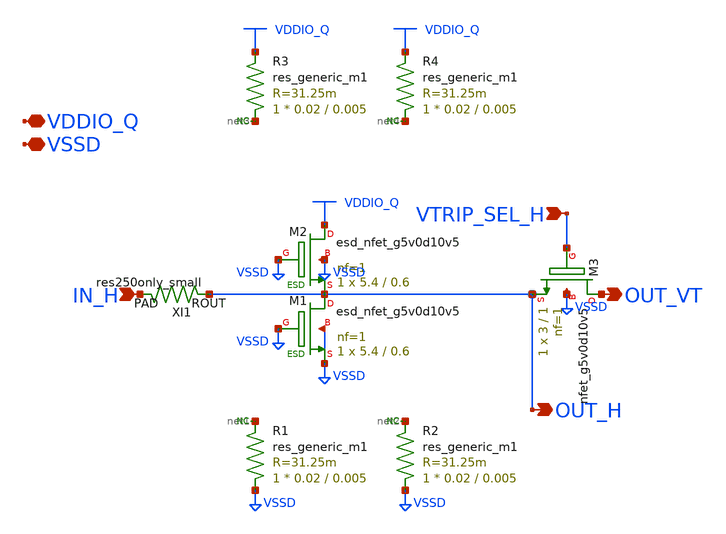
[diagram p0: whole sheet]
** sch_path: gpio_ovtv2_buf_localesd.sch
* Copyright 2023 David Mitchell Bailey
* Licensed under the Apache License, Version 2.0 (the "License");
* you may not use this file except in compliance with the License.
* You may obtain a copy of the License at
* https://www.apache.org/licenses/LICENSE-2.0
* Unless required by applicable law or agreed to in writing, software
* distributed under the License is distributed on an "AS IS" BASIS,
* WITHOUT WARRANTIES OR CONDITIONS OF ANY KIND, either express or implied.
* See the License for the specific language governing permissions and
* limitations under the License.
**.subckt gpio_ovtv2_buf_localesd IN_H VDDIO_Q OUT_VT VTRIP_SEL_H VSSD OUT_H
*.ipin IN_H
*.iopin VDDIO_Q
*.opin OUT_VT
*.ipin VTRIP_SEL_H
*.iopin VSSD
*.opin OUT_H
XM1 OUT_H VSSD VSSD VSSD sky130_fd_pr__esd_nfet_g5v0d10v5 L=0.6 W=5.4 nf=1 ad='int((nf+1)/2) * W/nf * 0.29'
+ as='int((nf+2)/2) * W/nf * 0.29' pd='2*int((nf+1)/2) * (W/nf + 0.29)' ps='2*int((nf+2)/2) * (W/nf + 0.29)'
+ nrd='0.29 / W' nrs='0.29 / W' sa=0 sb=0 sd=0 mult=1 m=1
XM2 VDDIO_Q VSSD OUT_H VSSD sky130_fd_pr__esd_nfet_g5v0d10v5 L=0.6 W=5.4 nf=1 ad='int((nf+1)/2) * W/nf * 0.29'
+ as='int((nf+2)/2) * W/nf * 0.29' pd='2*int((nf+1)/2) * (W/nf + 0.29)' ps='2*int((nf+2)/2) * (W/nf + 0.29)'
+ nrd='0.29 / W' nrs='0.29 / W' sa=0 sb=0 sd=0 mult=1 m=1
XM3 OUT_VT VTRIP_SEL_H OUT_H VSSD sky130_fd_pr__nfet_g5v0d10v5 L=1 W=3 nf=1 ad='int((nf+1)/2) * W/nf * 0.29'
+ as='int((nf+2)/2) * W/nf * 0.29' pd='2*int((nf+1)/2) * (W/nf + 0.29)' ps='2*int((nf+2)/2) * (W/nf + 0.29)'
+ nrd='0.29 / W' nrs='0.29 / W' sa=0 sb=0 sd=0 mult=1 m=1
R1 VSSD net1 sky130_fd_pr__res_generic_m1 W=0.02 L=0.005 m=1
XI1 OUT_H IN_H res250only_small
R2 VSSD net2 sky130_fd_pr__res_generic_m1 W=0.02 L=0.005 m=1
R3 net3 VDDIO_Q sky130_fd_pr__res_generic_m1 W=0.02 L=0.005 m=1
R4 net4 VDDIO_Q sky130_fd_pr__res_generic_m1 W=0.02 L=0.005 m=1
* noconn #net1
* noconn #net2
* noconn #net3
* noconn #net4
**.ends

* expanding   symbol:  res250only_small.sym # of pins=2
** sym_path: res250only_small.sym
** sch_path: res250only_small.sch
.subckt res250only_small ROUT PAD
*.iopin PAD
*.iopin ROUT
XR2 ROUT ROUT sky130_fd_pr__res_generic_po W=0.3 L=0.085 m=1
XR3 ROUT PAD sky130_fd_pr__res_generic_po W=2 L=10.07 m=1
XR4 PAD PAD sky130_fd_pr__res_generic_po W=0.3 L=0.085 m=1
R1 ROUT ROUT sky130_fd_pr__res_generic_l1 W=2 L=0.17 m=1
R5 PAD PAD sky130_fd_pr__res_generic_l1 W=2 L=0.17 m=1
R6 PAD PAD sky130_fd_pr__res_generic_m1 W=2 L=0.17 m=1
R7 ROUT ROUT sky130_fd_pr__res_generic_m1 W=2 L=0.17 m=1
XR8 ROUT ROUT sky130_fd_pr__res_generic_po W=0.34 L=0.085 m=1
XR9 PAD PAD sky130_fd_pr__res_generic_po W=0.34 L=0.085 m=1
.ends

.end
